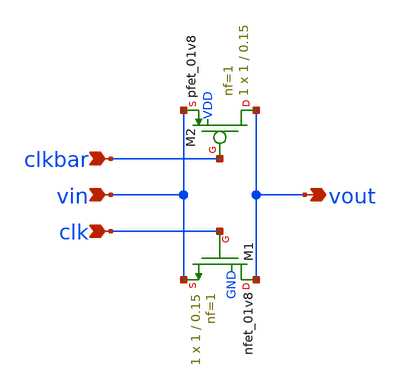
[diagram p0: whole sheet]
** sch_path: xschem/comparator/TG_ank.sch
**.subckt TG_ank clkbar vout vin clk
*.ipin clkbar
*.opin vout
*.ipin vin
*.ipin clk
XM1 vout clk vin GND sky130_fd_pr__nfet_01v8 L=0.15 W=1 nf=1 ad='int((nf+1)/2) * W/nf * 0.29' as='int((nf+2)/2) * W/nf * 0.29'
+ pd='2*int((nf+1)/2) * (W/nf + 0.29)' ps='2*int((nf+2)/2) * (W/nf + 0.29)' nrd='0.29 / W' nrs='0.29 / W'
+ sa=0 sb=0 sd=0 mult=1 m=1
XM2 vout clkbar vin VDD sky130_fd_pr__pfet_01v8 L=0.15 W=1 nf=1 ad='int((nf+1)/2) * W/nf * 0.29' as='int((nf+2)/2) * W/nf * 0.29'
+ pd='2*int((nf+1)/2) * (W/nf + 0.29)' ps='2*int((nf+2)/2) * (W/nf + 0.29)' nrd='0.29 / W' nrs='0.29 / W'
+ sa=0 sb=0 sd=0 mult=1 m=1
**.ends
.end
